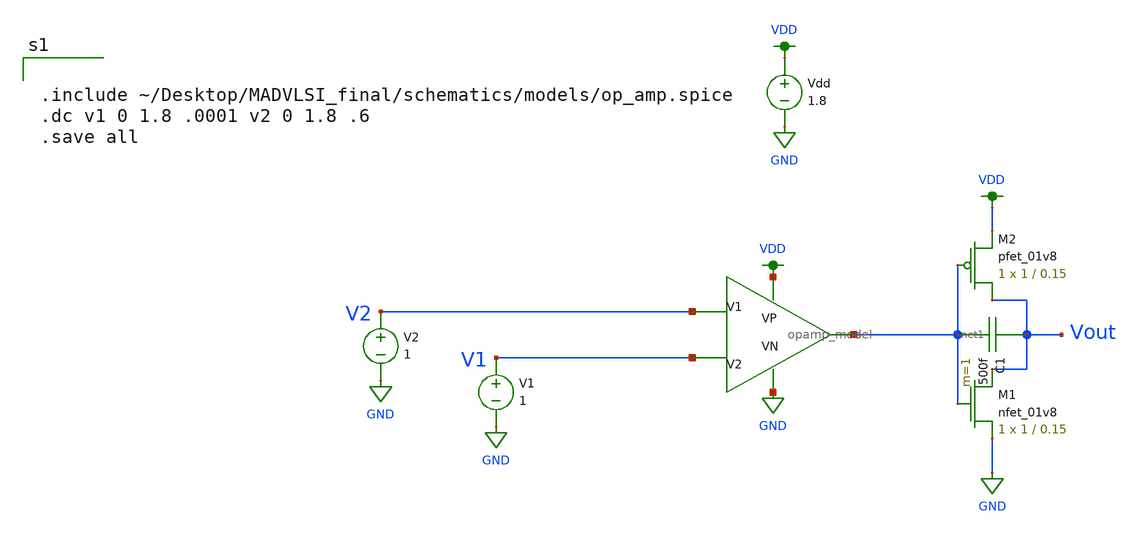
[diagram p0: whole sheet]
** sch_path: schematics/old/opamp_ideal_testbench.sch
**.subckt opamp_ideal_testbench
Vdd VDD GND 1.8
X1 V2 V1 VDD GND net1 opamp_model
V1 V1 GND 1
V2 V2 GND 1
XM1 Vout net1 GND GND sky130_fd_pr__nfet_01v8 L=0.15 W=1 nf=1 ad='int((nf+1)/2) * W/nf * 0.29' as='int((nf+2)/2) * W/nf * 0.29'
+ pd='2*int((nf+1)/2) * (W/nf + 0.29)' ps='2*int((nf+2)/2) * (W/nf + 0.29)' nrd='0.29 / W' nrs='0.29 / W'
+ sa=0 sb=0 sd=0 mult=1 m=1
XM2 Vout net1 VDD VDD sky130_fd_pr__pfet_01v8 L=0.15 W=1 nf=1 ad='int((nf+1)/2) * W/nf * 0.29' as='int((nf+2)/2) * W/nf * 0.29'
+ pd='2*int((nf+1)/2) * (W/nf + 0.29)' ps='2*int((nf+2)/2) * (W/nf + 0.29)' nrd='0.29 / W' nrs='0.29 / W'
+ sa=0 sb=0 sd=0 mult=1 m=1
C1 Vout net1 500f m=1
**** begin user architecture code


.include ~/Desktop/MADVLSI_final/schematics/models/op_amp.spice
.dc v1 0 1.8 .0001 v2 0 1.8 .6
.save all


.option wnflag=1
.param MC_SWITCH=0.0
.lib ~/skywater/skywater-pdk/libraries/sky130_fd_pr_ngspice/latest/models/sky130.lib.spice tt

**** end user architecture code
**.ends
.GLOBAL GND
.GLOBAL VDD
.end
